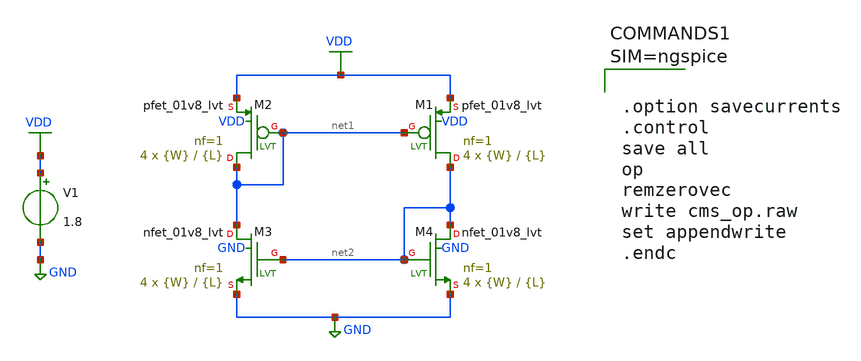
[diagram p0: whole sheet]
** sch_path: xschem/cms_op.sch
**.subckt cms_op
XM1 net2 net1 VDD VDD sky130_fd_pr__pfet_01v8_lvt L={L} W={W} nf=1 ad='int((nf+1)/2) * W/nf * 0.29' as='int((nf+2)/2) * W/nf * 0.29'
+ pd='2*int((nf+1)/2) * (W/nf + 0.29)' ps='2*int((nf+2)/2) * (W/nf + 0.29)' nrd='0.29 / W' nrs='0.29 / W'
+ sa=0 sb=0 sd=0 mult=4 m=4
XM2 net1 net1 VDD VDD sky130_fd_pr__pfet_01v8_lvt L={L} W={W} nf=1 ad='int((nf+1)/2) * W/nf * 0.29' as='int((nf+2)/2) * W/nf * 0.29'
+ pd='2*int((nf+1)/2) * (W/nf + 0.29)' ps='2*int((nf+2)/2) * (W/nf + 0.29)' nrd='0.29 / W' nrs='0.29 / W'
+ sa=0 sb=0 sd=0 mult=4 m=4
XM3 net1 net2 GND GND sky130_fd_pr__nfet_01v8_lvt L={L} W={W} nf=1 ad='int((nf+1)/2) * W/nf * 0.29' as='int((nf+2)/2) * W/nf * 0.29'
+ pd='2*int((nf+1)/2) * (W/nf + 0.29)' ps='2*int((nf+2)/2) * (W/nf + 0.29)' nrd='0.29 / W' nrs='0.29 / W'
+ sa=0 sb=0 sd=0 mult=4 m=4
XM4 net2 net2 GND GND sky130_fd_pr__nfet_01v8_lvt L={L} W={W} nf=1 ad='int((nf+1)/2) * W/nf * 0.29' as='int((nf+2)/2) * W/nf * 0.29'
+ pd='2*int((nf+1)/2) * (W/nf + 0.29)' ps='2*int((nf+2)/2) * (W/nf + 0.29)' nrd='0.29 / W' nrs='0.29 / W'
+ sa=0 sb=0 sd=0 mult=4 m=4
V1 VDD GND 1.8
**** begin user architecture code

** opencircuitdesign pdks install
.lib $::SKYWATER_MODELS/sky130.lib.spice tt




.param L=5.8
.param W=1





.option savecurrents
.control
save all
op
remzerovec
write cms_op.raw
set appendwrite
.endc



**** end user architecture code
**.ends
.GLOBAL VDD
.GLOBAL GND
.end
